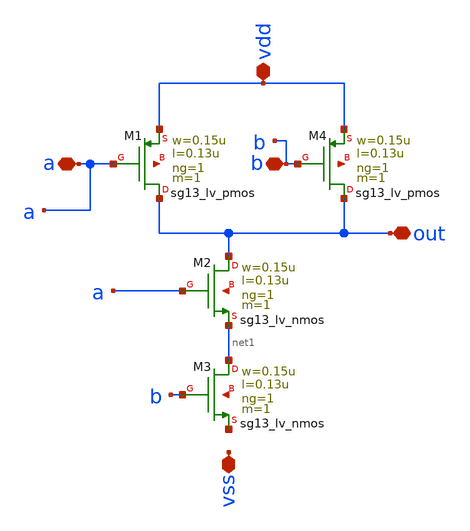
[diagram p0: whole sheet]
** sch_path: design/blocks/nandgate/schematic/nand.sch
**.subckt nand vdd a vss out b
*.iopin vdd
*.iopin a
*.iopin vss
*.iopin out
*.iopin b
XM1 out a vdd net2 sg13_lv_pmos w=0.15u l=0.13u ng=1 m=1 mm_ok=1
XM2 out a net1 net3 sg13_lv_nmos w=0.15u l=0.13u ng=1 m=1 mm_ok=1
XM3 net1 b net4 net5 sg13_lv_nmos w=0.15u l=0.13u ng=1 m=1 mm_ok=1
XM4 out b vdd net6 sg13_lv_pmos w=0.15u l=0.13u ng=1 m=1 mm_ok=1
**.ends
.end
